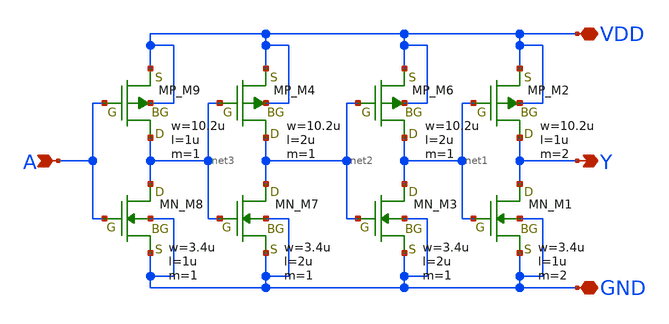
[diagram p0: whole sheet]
** sch_path: libs.tech/xschem/TR-1um_5_stdcell/DEL1.sch
**.subckt DEL1 A Y VDD GND
*.ipin A
*.opin Y
*.iopin VDD
*.iopin GND
XM9 net3 A VDD VDD PMOS w=10.2u l=1u nrd=0 nrs=0 m=1
XM2 Y net1 VDD VDD PMOS w=10.2u l=1u nrd=0 nrs=0 m=2
XM8 net3 A GND GND NMOS w=3.4u l=1u nrd=0 nrs=0 m=1
XM1 Y net1 GND GND NMOS w=3.4u l=1u nrd=0 nrs=0 m=2
XM4 net2 net3 VDD VDD PMOS w=10.2u l=2u nrd=0 nrs=0 m=1
XM6 net1 net2 VDD VDD PMOS w=10.2u l=2u nrd=0 nrs=0 m=1
XM7 net2 net3 GND GND NMOS w=3.4u l=2u nrd=0 nrs=0 m=1
XM3 net1 net2 GND GND NMOS w=3.4u l=2u nrd=0 nrs=0 m=1
**.ends
.end
